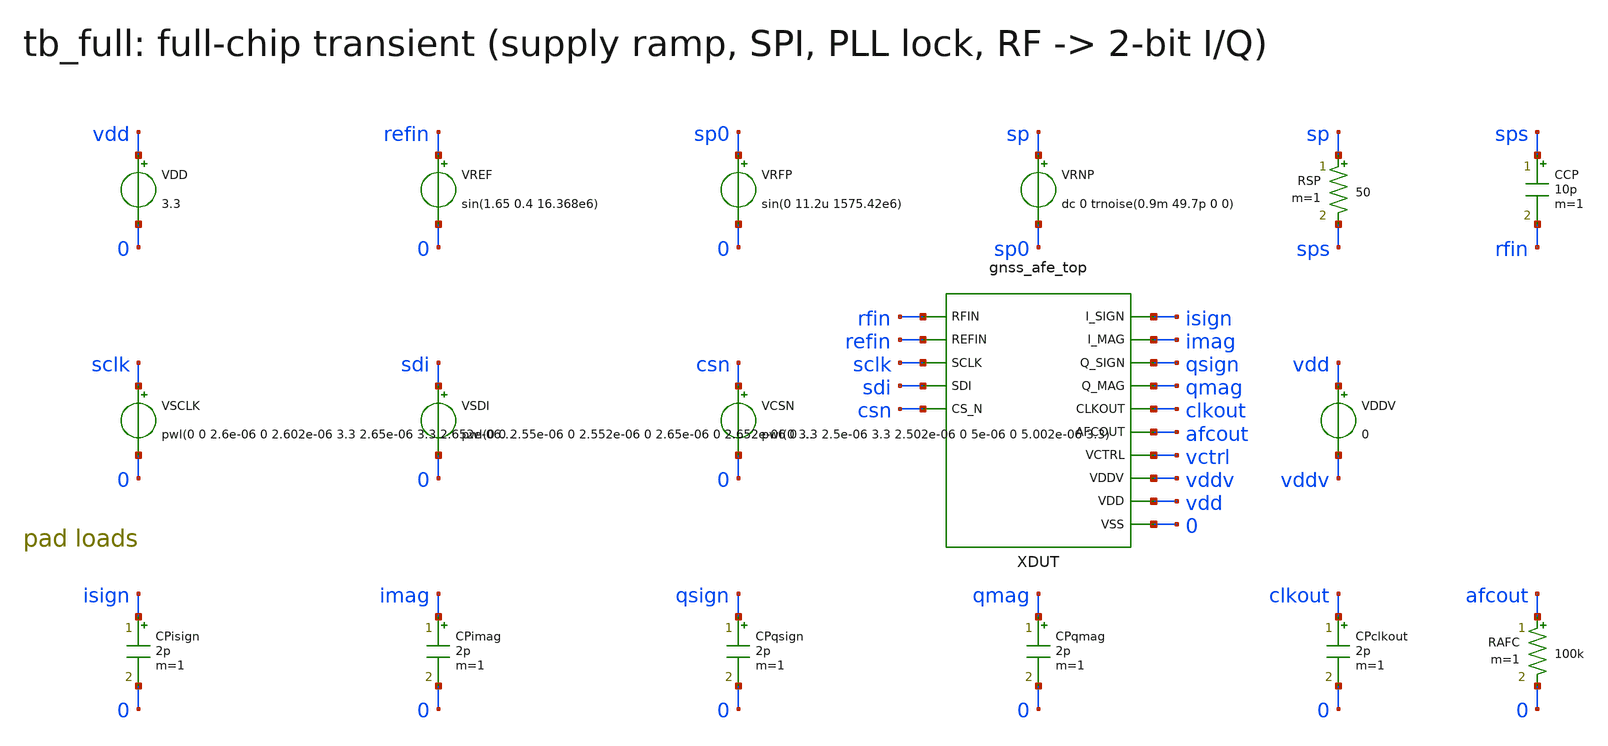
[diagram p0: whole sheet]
** sch_path: v1_claude/xschem/tb_full.sch
**.subckt tb_full
VDD vdd 0 3.3
VREF refin 0 sin(1.65 0.4 16.368e6)
VRFP sp0 0 sin(0 11.2u 1575.42e6)
VRNP sp sp0 dc 0 trnoise(0.9m 49.7p 0 0)
RSP sp sps 50 m=1
CCP sps rfin 10p m=1
VSCLK sclk 0 pwl(0 0 2.6e-06 0 2.602e-06 3.3 2.65e-06 3.3 2.652e-06 0 2.7e-06 0 2.702e-06 3.3
+ 2.75e-06 3.3 2.752e-06 0 2.8e-06 0 2.802e-06 3.3 2.85e-06 3.3 2.852e-06 0 2.9e-06 0 2.902e-06 3.3 2.95e-06
+ 3.3 2.952e-06 0 3e-06 0 3.002e-06 3.3 3.05e-06 3.3 3.052e-06 0 3.1e-06 0 3.102e-06 3.3 3.15e-06 3.3
+ 3.152e-06 0 3.2e-06 0 3.202e-06 3.3 3.25e-06 3.3 3.252e-06 0 3.3e-06 0 3.302e-06 3.3 3.35e-06 3.3 3.352e-06 0
+ 3.4e-06 0 3.402e-06 3.3 3.45e-06 3.3 3.452e-06 0 3.5e-06 0 3.502e-06 3.3 3.55e-06 3.3 3.552e-06 0 3.6e-06 0
+ 3.602e-06 3.3 3.65e-06 3.3 3.652e-06 0 3.7e-06 0 3.702e-06 3.3 3.75e-06 3.3 3.752e-06 0 3.8e-06 0 3.802e-06
+ 3.3 3.85e-06 3.3 3.852e-06 0 3.9e-06 0 3.902e-06 3.3 3.95e-06 3.3 3.952e-06 0 4e-06 0 4.002e-06 3.3
+ 4.05e-06 3.3 4.052e-06 0 4.1e-06 0 4.102e-06 3.3 4.15e-06 3.3 4.152e-06 0 4.2e-06 0 4.202e-06 3.3 4.25e-06
+ 3.3 4.252e-06 0 4.3e-06 0 4.302e-06 3.3 4.35e-06 3.3 4.352e-06 0 4.4e-06 0 4.402e-06 3.3 4.45e-06 3.3
+ 4.452e-06 0 4.5e-06 0 4.502e-06 3.3 4.55e-06 3.3 4.552e-06 0 4.6e-06 0 4.602e-06 3.3 4.65e-06 3.3 4.652e-06 0
+ 4.7e-06 0 4.702e-06 3.3 4.75e-06 3.3 4.752e-06 0 4.8e-06 0 4.802e-06 3.3 4.85e-06 3.3 4.852e-06 0 4.9e-06 0
+ 4.902e-06 3.3 4.95e-06 3.3 4.952e-06 0)
VSDI sdi 0 pwl(0 0 2.55e-06 0 2.552e-06 0 2.65e-06 0 2.652e-06 0 2.75e-06 0 2.752e-06 0 2.85e-06 0
+ 2.852e-06 0 2.95e-06 0 2.952e-06 0 3.05e-06 0 3.052e-06 0 3.15e-06 0 3.152e-06 0 3.25e-06 0 3.252e-06 0
+ 3.35e-06 0 3.352e-06 0 3.45e-06 0 3.452e-06 0 3.55e-06 0 3.552e-06 0 3.65e-06 0 3.652e-06 0 3.75e-06 0
+ 3.752e-06 0 3.85e-06 0 3.852e-06 0 3.95e-06 0 3.952e-06 0 4.05e-06 0 4.052e-06 0 4.15e-06 0 4.152e-06 0
+ 4.25e-06 0 4.252e-06 0 4.35e-06 0 4.352e-06 0 4.45e-06 0 4.452e-06 3.3 4.55e-06 3.3 4.552e-06 0 4.65e-06 0
+ 4.652e-06 3.3 4.75e-06 3.3 4.752e-06 0 4.85e-06 0 4.852e-06 3.3)
VCSN csn 0 pwl(0 3.3 2.5e-06 3.3 2.502e-06 0 5e-06 0 5.002e-06 3.3)
XDUT rfin refin sclk sdi csn isign imag qsign qmag clkout afcout vctrl vddv vdd 0 gnss_afe_top
VDDV vdd vddv 0
CPisign isign 0 2p m=1
CPimag imag 0 2p m=1
CPqsign qsign 0 2p m=1
CPqmag qmag 0 2p m=1
CPclkout clkout 0 2p m=1
RAFC afcout 0 100k m=1
**** begin user architecture code
 .include $::180MCU_MODELS/design.ngspice
.lib $::180MCU_MODELS/sm141064.ngspice typical
.lib $::180MCU_MODELS/sm141064.ngspice res_typical
.lib $::180MCU_MODELS/sm141064.ngspice mimcap_typical

.option method=gear reltol=2e-4 minbreak=1e-12
.ic v(xdut.vctrl)=1.7 v(xdut.xpll.xlf.z)=1.7 v(xdut.xpll.vcp)=1.7 v(xdut.xvco.xcore.p4)=0
+ v(xdut.xvco.xcore.n4)=1
.control
set num_threads=1
save v(vctrl) v(xdut.vctrl) v(clkout) v(isign) v(imag) v(qsign) v(qmag) v(afcout) v(xdut.aip)
+ v(xdut.ain) v(xdut.aqp) v(xdut.aqn) v(xdut.mip) v(xdut.min) v(xdut.mqp) v(xdut.mqn) v(rfin) v(xdut.rfp)
+ v(xdut.rfn) i(VDD)
tran 5p 12u 0 5p uic
wrdata tb_full_out v(vctrl) v(clkout) v(isign) v(imag) v(qsign) v(qmag) v(xdut.aip,xdut.ain)
+ v(xdut.aqp,xdut.aqn) v(xdut.mip,xdut.min) v(xdut.mqp,xdut.mqn) v(rfin) v(xdut.rfp,xdut.rfn) i(VDD)
meas tran vc_end avg v(vctrl) from=11u to=12u
meas tran idd avg i(VDD) from=8u to=12u
echo RES vc_end=$&vc_end idd=$&idd
.endc

**** end user architecture code
**.ends
.end
